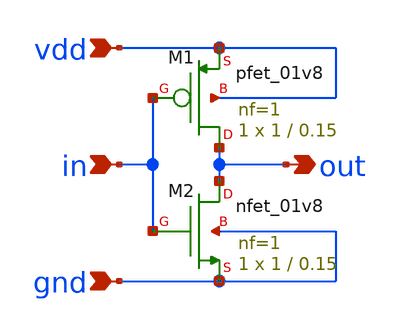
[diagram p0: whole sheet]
** sch_path: Inverter/inverter2.sch
**.subckt inverter2 in out vdd gnd
*.ipin in
*.opin out
*.ipin vdd
*.ipin gnd
XM1 out in vdd vdd sky130_fd_pr__pfet_01v8 L=0.15 W=1 nf=1 ad='int((nf+1)/2) * W/nf * 0.29' as='int((nf+2)/2) * W/nf * 0.29'
+ pd='2*int((nf+1)/2) * (W/nf + 0.29)' ps='2*int((nf+2)/2) * (W/nf + 0.29)' nrd='0.29 / W' nrs='0.29 / W'
+ sa=0 sb=0 sd=0 mult=1 m=1
XM2 out in gnd gnd sky130_fd_pr__nfet_01v8 L=0.15 W=1 nf=1 ad='int((nf+1)/2) * W/nf * 0.29' as='int((nf+2)/2) * W/nf * 0.29'
+ pd='2*int((nf+1)/2) * (W/nf + 0.29)' ps='2*int((nf+2)/2) * (W/nf + 0.29)' nrd='0.29 / W' nrs='0.29 / W'
+ sa=0 sb=0 sd=0 mult=1 m=1
**.ends
.end
